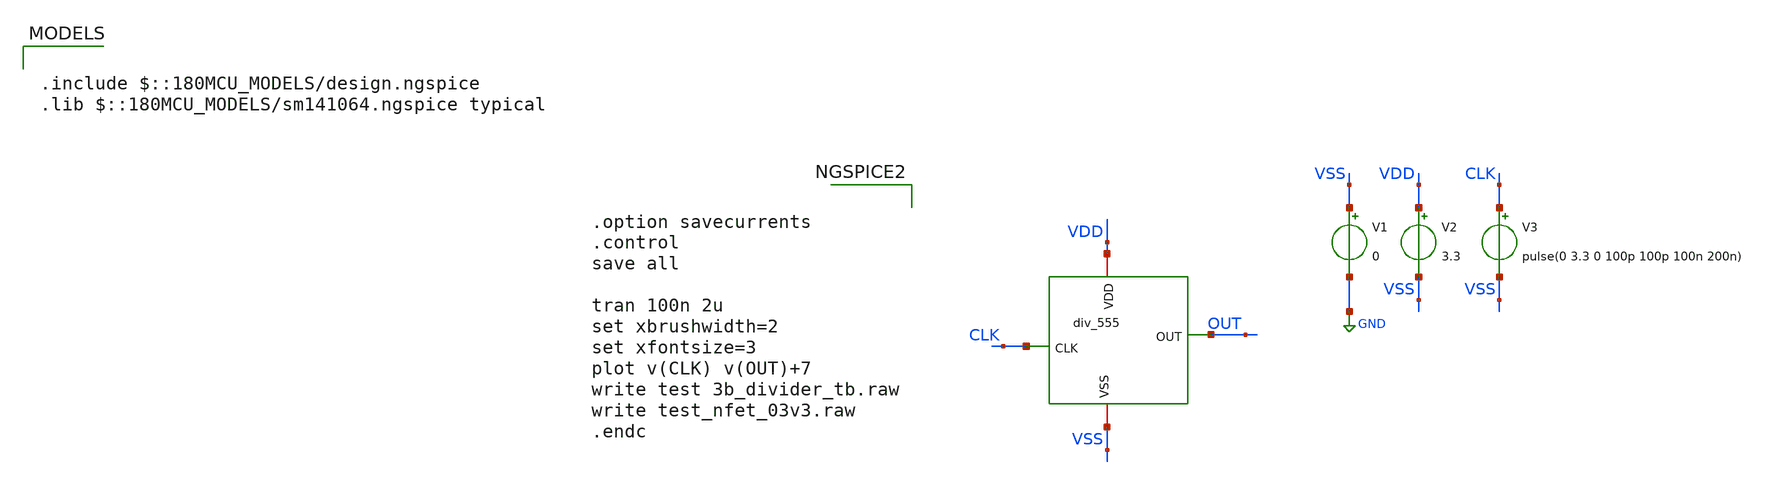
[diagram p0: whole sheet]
** sch_path: Clock_Generator_PAKISTAN_06/Schematics/div555_tb.sch
**.subckt div555_tb
x1 VDD CLK OUT VSS div_555
V1 VSS GND 0
V2 VDD VSS 3.3
V3 CLK VSS pulse(0 3.3 0 100p 100p 100n 200n)
**** begin user architecture code

.include $::180MCU_MODELS/design.ngspice
.lib $::180MCU_MODELS/sm141064.ngspice typical



.option savecurrents
.control
save all

tran 100n 2u
set xbrushwidth=2
set xfontsize=3
plot v(CLK) v(OUT)+7
write test 3b_divider_tb.raw
write test_nfet_03v3.raw
.endc


**** end user architecture code
**.ends
.GLOBAL GND
.end
